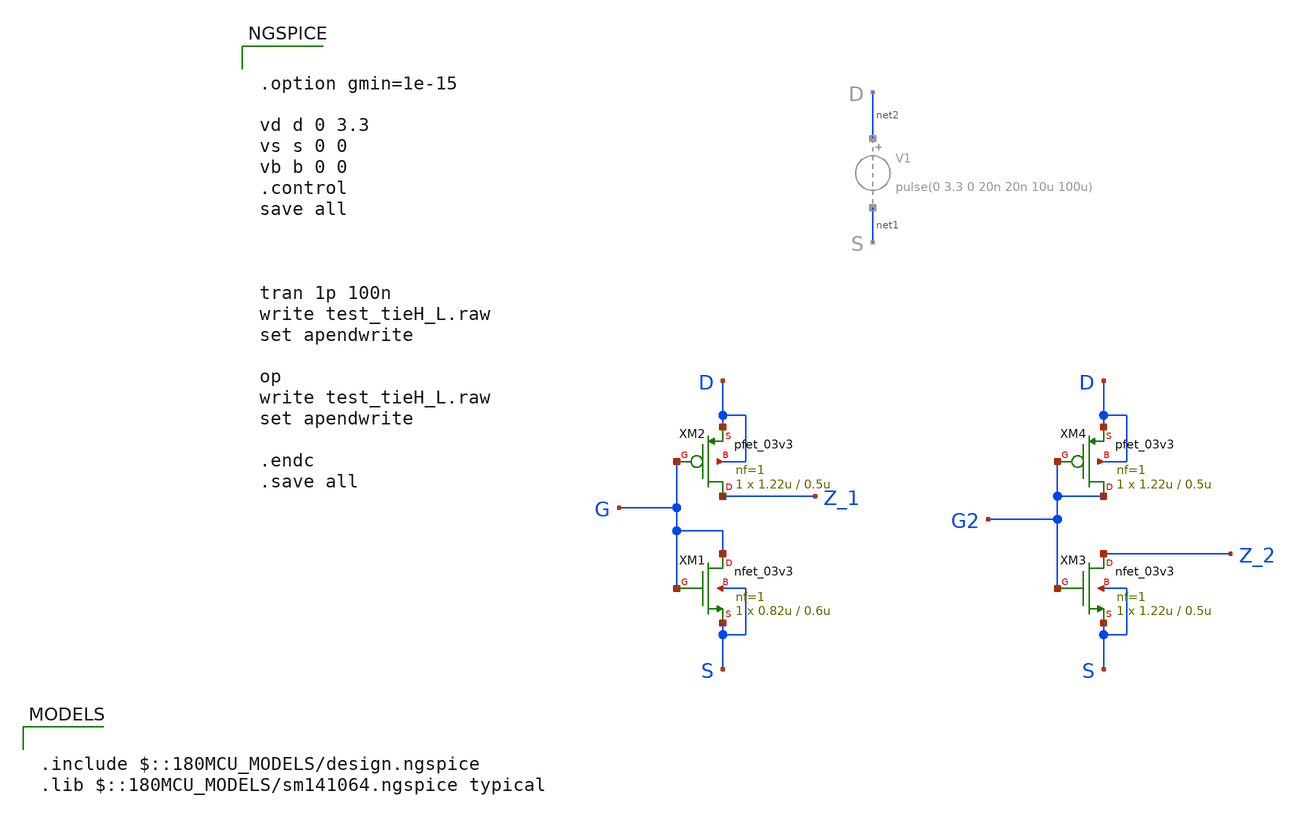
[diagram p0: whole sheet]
** sch_path: designs/Chipathon2025_pads/xschem/test_tieH_L.sch
**.subckt test_tieH_L
XM1 G G S S nfet_03v3 L=0.6u W=0.82u nf=1 ad='int((nf+1)/2) * W/nf * 0.18u' as='int((nf+2)/2) * W/nf * 0.18u'
+ pd='2*int((nf+1)/2) * (W/nf + 0.18u)' ps='2*int((nf+2)/2) * (W/nf + 0.18u)' nrd='0.18u / W' nrs='0.18u / W'
+ sa=0 sb=0 sd=0 m=1
XM2 Z_1 G D D pfet_03v3 L=0.5u W=1.22u nf=1 ad='int((nf+1)/2) * W/nf * 0.18u' as='int((nf+2)/2) * W/nf * 0.18u'
+ pd='2*int((nf+1)/2) * (W/nf + 0.18u)' ps='2*int((nf+2)/2) * (W/nf + 0.18u)' nrd='0.18u / W' nrs='0.18u / W'
+ sa=0 sb=0 sd=0 m=1
XM3 Z_2 G2 S S nfet_03v3 L=0.5u W=1.22u nf=1 ad='int((nf+1)/2) * W/nf * 0.18u' as='int((nf+2)/2) * W/nf * 0.18u'
+ pd='2*int((nf+1)/2) * (W/nf + 0.18u)' ps='2*int((nf+2)/2) * (W/nf + 0.18u)' nrd='0.18u / W' nrs='0.18u / W'
+ sa=0 sb=0 sd=0 m=1
XM4 G2 G2 D D pfet_03v3 L=0.5u W=1.22u nf=1 ad='int((nf+1)/2) * W/nf * 0.18u' as='int((nf+2)/2) * W/nf * 0.18u'
+ pd='2*int((nf+1)/2) * (W/nf + 0.18u)' ps='2*int((nf+2)/2) * (W/nf + 0.18u)' nrd='0.18u / W' nrs='0.18u / W'
+ sa=0 sb=0 sd=0 m=1
**** begin user architecture code

.include $::180MCU_MODELS/design.ngspice
.lib $::180MCU_MODELS/sm141064.ngspice typical



.option gmin=1e-15

vd d 0 3.3
vs s 0 0
vb b 0 0
.control
save all



tran 1p 100n
write test_tieH_L.raw
set apendwrite

op
write test_tieH_L.raw
set apendwrite

.endc
.save all


**** end user architecture code
**.ends
.end
